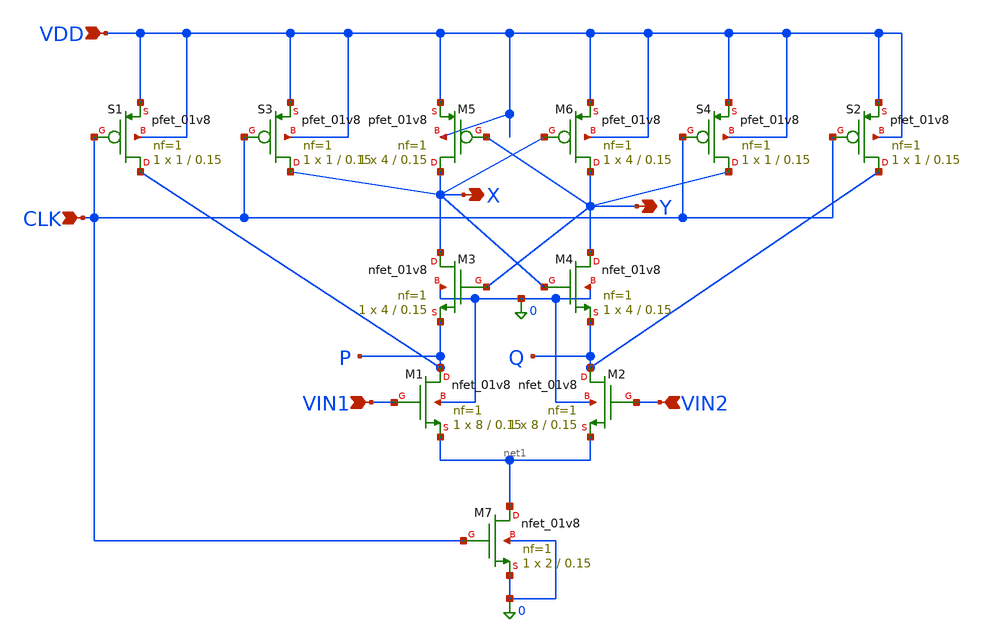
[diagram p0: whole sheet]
** sch_path: strongarm_comparator.sch
**.subckt strongarm_comparator VDD CLK VIN1 VIN2 X Y
*.ipin VDD
*.ipin CLK
*.ipin VIN1
*.ipin VIN2
*.opin X
*.opin Y
XS1 P CLK VDD VDD sky130_fd_pr__pfet_01v8 L=0.15 W=1 nf=1 ad='int((nf+1)/2) * W/nf * 0.29' as='int((nf+2)/2) * W/nf * 0.29'
+ pd='2*int((nf+1)/2) * (W/nf + 0.29)' ps='2*int((nf+2)/2) * (W/nf + 0.29)' nrd='0.29 / W' nrs='0.29 / W'
+ sa=0 sb=0 sd=0 mult=1 m=1
XS3 X CLK VDD VDD sky130_fd_pr__pfet_01v8 L=0.15 W=1 nf=1 ad='int((nf+1)/2) * W/nf * 0.29' as='int((nf+2)/2) * W/nf * 0.29'
+ pd='2*int((nf+1)/2) * (W/nf + 0.29)' ps='2*int((nf+2)/2) * (W/nf + 0.29)' nrd='0.29 / W' nrs='0.29 / W'
+ sa=0 sb=0 sd=0 mult=1 m=1
XM5 X Y VDD VDD sky130_fd_pr__pfet_01v8 L=0.15 W=4 nf=1 ad='int((nf+1)/2) * W/nf * 0.29' as='int((nf+2)/2) * W/nf * 0.29'
+ pd='2*int((nf+1)/2) * (W/nf + 0.29)' ps='2*int((nf+2)/2) * (W/nf + 0.29)' nrd='0.29 / W' nrs='0.29 / W'
+ sa=0 sb=0 sd=0 mult=1 m=1
XM6 Y X VDD VDD sky130_fd_pr__pfet_01v8 L=0.15 W=4 nf=1 ad='int((nf+1)/2) * W/nf * 0.29' as='int((nf+2)/2) * W/nf * 0.29'
+ pd='2*int((nf+1)/2) * (W/nf + 0.29)' ps='2*int((nf+2)/2) * (W/nf + 0.29)' nrd='0.29 / W' nrs='0.29 / W'
+ sa=0 sb=0 sd=0 mult=1 m=1
XS4 Y CLK VDD VDD sky130_fd_pr__pfet_01v8 L=0.15 W=1 nf=1 ad='int((nf+1)/2) * W/nf * 0.29' as='int((nf+2)/2) * W/nf * 0.29'
+ pd='2*int((nf+1)/2) * (W/nf + 0.29)' ps='2*int((nf+2)/2) * (W/nf + 0.29)' nrd='0.29 / W' nrs='0.29 / W'
+ sa=0 sb=0 sd=0 mult=1 m=1
XS2 Q CLK VDD VDD sky130_fd_pr__pfet_01v8 L=0.15 W=1 nf=1 ad='int((nf+1)/2) * W/nf * 0.29' as='int((nf+2)/2) * W/nf * 0.29'
+ pd='2*int((nf+1)/2) * (W/nf + 0.29)' ps='2*int((nf+2)/2) * (W/nf + 0.29)' nrd='0.29 / W' nrs='0.29 / W'
+ sa=0 sb=0 sd=0 mult=1 m=1
XM4 Y X Q 0 sky130_fd_pr__nfet_01v8 L=0.15 W=4 nf=1 ad='int((nf+1)/2) * W/nf * 0.29' as='int((nf+2)/2) * W/nf * 0.29'
+ pd='2*int((nf+1)/2) * (W/nf + 0.29)' ps='2*int((nf+2)/2) * (W/nf + 0.29)' nrd='0.29 / W' nrs='0.29 / W'
+ sa=0 sb=0 sd=0 mult=1 m=1
XM3 X Y P 0 sky130_fd_pr__nfet_01v8 L=0.15 W=4 nf=1 ad='int((nf+1)/2) * W/nf * 0.29' as='int((nf+2)/2) * W/nf * 0.29'
+ pd='2*int((nf+1)/2) * (W/nf + 0.29)' ps='2*int((nf+2)/2) * (W/nf + 0.29)' nrd='0.29 / W' nrs='0.29 / W'
+ sa=0 sb=0 sd=0 mult=1 m=1
XM1 P VIN1 net1 0 sky130_fd_pr__nfet_01v8 L=0.15 W=8 nf=1 ad='int((nf+1)/2) * W/nf * 0.29' as='int((nf+2)/2) * W/nf * 0.29'
+ pd='2*int((nf+1)/2) * (W/nf + 0.29)' ps='2*int((nf+2)/2) * (W/nf + 0.29)' nrd='0.29 / W' nrs='0.29 / W'
+ sa=0 sb=0 sd=0 mult=1 m=1
XM2 Q VIN2 net1 0 sky130_fd_pr__nfet_01v8 L=0.15 W=8 nf=1 ad='int((nf+1)/2) * W/nf * 0.29' as='int((nf+2)/2) * W/nf * 0.29'
+ pd='2*int((nf+1)/2) * (W/nf + 0.29)' ps='2*int((nf+2)/2) * (W/nf + 0.29)' nrd='0.29 / W' nrs='0.29 / W'
+ sa=0 sb=0 sd=0 mult=1 m=1
XM7 net1 CLK 0 0 sky130_fd_pr__nfet_01v8 L=0.15 W=2 nf=1 ad='int((nf+1)/2) * W/nf * 0.29' as='int((nf+2)/2) * W/nf * 0.29'
+ pd='2*int((nf+1)/2) * (W/nf + 0.29)' ps='2*int((nf+2)/2) * (W/nf + 0.29)' nrd='0.29 / W' nrs='0.29 / W'
+ sa=0 sb=0 sd=0 mult=1 m=1
**.ends
.end
